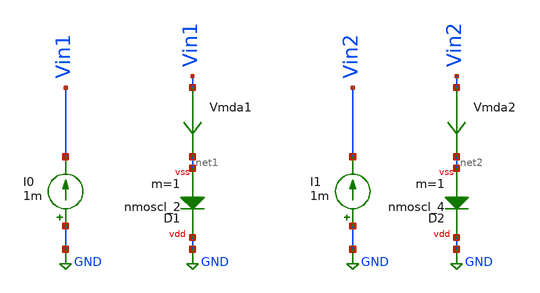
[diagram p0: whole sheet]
** sch_path: ihp-sg13g2/xschem_libs/sg13g2_tests_ase/dc_esd_nmos_cl/schematic/dc_esd_nmos_cl.sch
**.subckt dc_esd_nmos_cl
Vmda1 Vin1 net1 0
.save i(vmda1)
I0 GND Vin1 1m
Vmda2 Vin2 net2 0
.save i(vmda2)
I1 GND Vin2 1m
XD1 GND net1 nmoscl_2 m=1
XD2 GND net2 nmoscl_4 m=1
**.ends
.GLOBAL GND
.end
